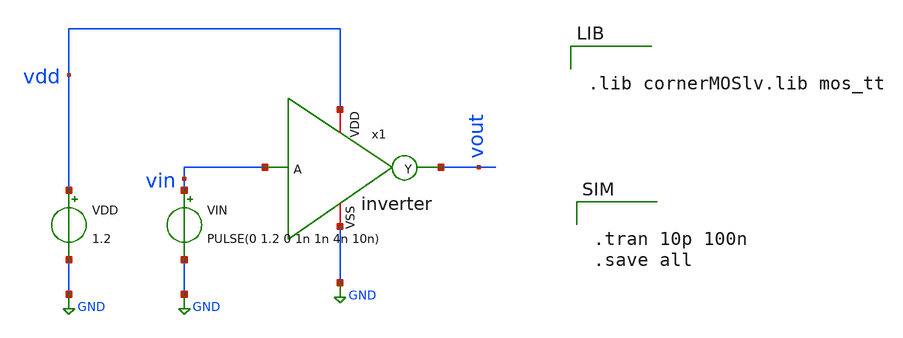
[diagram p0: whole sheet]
** sch_path: BTDay6-Ex/inverter_sym.sch
**.subckt inverter_sym
VIN vin GND PULSE(0 1.2 0 1n 1n 4n 10n)
VDD vdd GND 1.2
x1 vdd vin vout GND inverter
**** begin user architecture code


.lib cornerMOSlv.lib mos_tt




.tran 10p 100n
.save all


**** end user architecture code
**.ends

* expanding   symbol:  /foss/designs/BTDay6-Ex/inverter.sym # of pins=4
** sym_path: BTDay6-Ex/inverter.sym
** sch_path: BTDay6-Ex/inverter.sch
.subckt inverter VDD A Y VSS
*.ipin A
*.opin Y
*.iopin VDD
*.iopin VSS
XM1 Y A VSS VSS sg13_lv_nmos w=0.15u l=0.13u ng=1 m=1 mm_ok=1
XM2 Y A VDD VDD sg13_lv_pmos w=0.15u l=0.13u ng=1 m=1 mm_ok=1
.ends

.GLOBAL GND
.end
